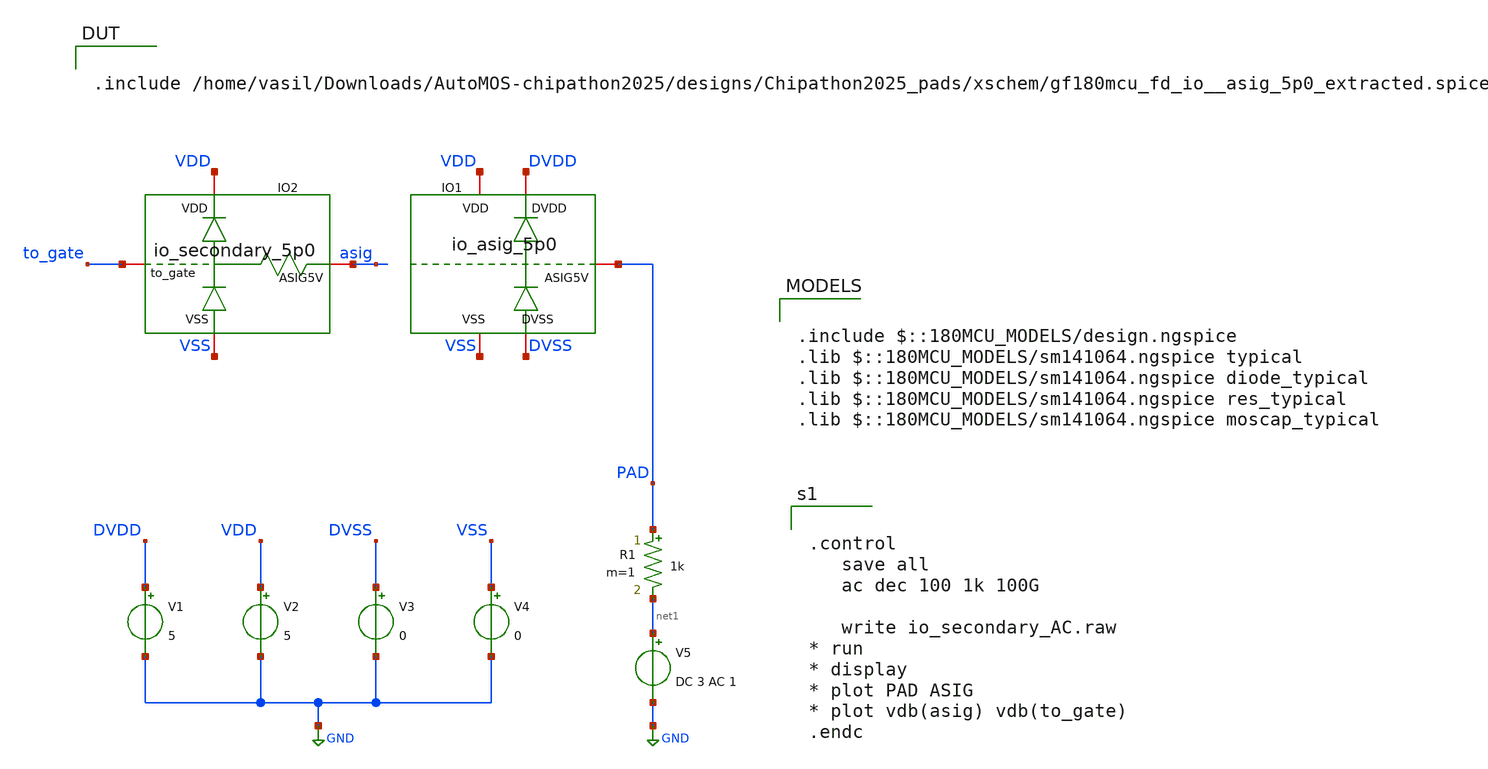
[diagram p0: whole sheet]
** sch_path: designs/Chipathon2025_pads/xschem/io_secondary_AC_tb.sch
**.subckt io_secondary_AC_tb
V1 DVDD GND 5
V2 VDD GND 5
V3 DVSS GND 0
V4 VSS GND 0
V5 net1 GND DC 3 AC 1
R1 PAD net1 1k m=1
XIO1 PAD DVDD DVSS VDD VSS gf180mcu_fd_io__asig_5p0_extracted
XIO2 VDD to_gate asig VSS io_secondary_5p0
**** begin user architecture code

.include $::180MCU_MODELS/design.ngspice
.lib $::180MCU_MODELS/sm141064.ngspice typical
.lib $::180MCU_MODELS/sm141064.ngspice diode_typical
.lib $::180MCU_MODELS/sm141064.ngspice res_typical
.lib $::180MCU_MODELS/sm141064.ngspice moscap_typical



.control
   save all
   ac dec 100 1k 100G

   write io_secondary_AC.raw
* run
* display
* plot PAD ASIG
* plot vdb(asig) vdb(to_gate)
.endc



.include /home/vasil/Downloads/AutoMOS-chipathon2025/designs/Chipathon2025_pads/xschem/gf180mcu_fd_io__asig_5p0_extracted.spice

**** end user architecture code
**.ends

* expanding   symbol:  Chipathon2025_pads/xschem/symbols/io_asig_5p0.sym # of pins=5
** sym_path: designs/Chipathon2025_pads/xschem/symbols/io_asig_5p0.sym
.include /foss/designs/libs/Chipathon2025_pads/xschem/gf180mcu_fd_io.spice

* expanding   symbol:  Chipathon2025_pads/xschem/symbols/io_secondary_5p0/io_secondary_5p0.sym # of
*+ pins=4
** sym_path: Chipathon2025_pads/xschem/symbols/io_secondary_5p0/io_secondary_5p0.sym
** sch_path: Chipathon2025_pads/xschem/symbols/io_secondary_5p0/io_secondary_5p0.sch
.subckt io_secondary_5p0 VDD to_gate ASIG5V VSS


*.iopin VSS
*.iopin VDD
*.iopin to_gate
*.iopin ASIG5V
D1 to_gate VDD diode_pd2nw_06v0 area='10u * 10u ' pj='2*10u + 2*10u ' m=4
XR1 to_gate ASIG5V VDD ppolyf_u r_width=40e-6 r_length=10e-6 m=1
D2 VSS to_gate diode_nd2ps_06v0 area='10u * 10u ' pj='2*10u + 2*10u ' m=4
.ends

.GLOBAL GND
.end
